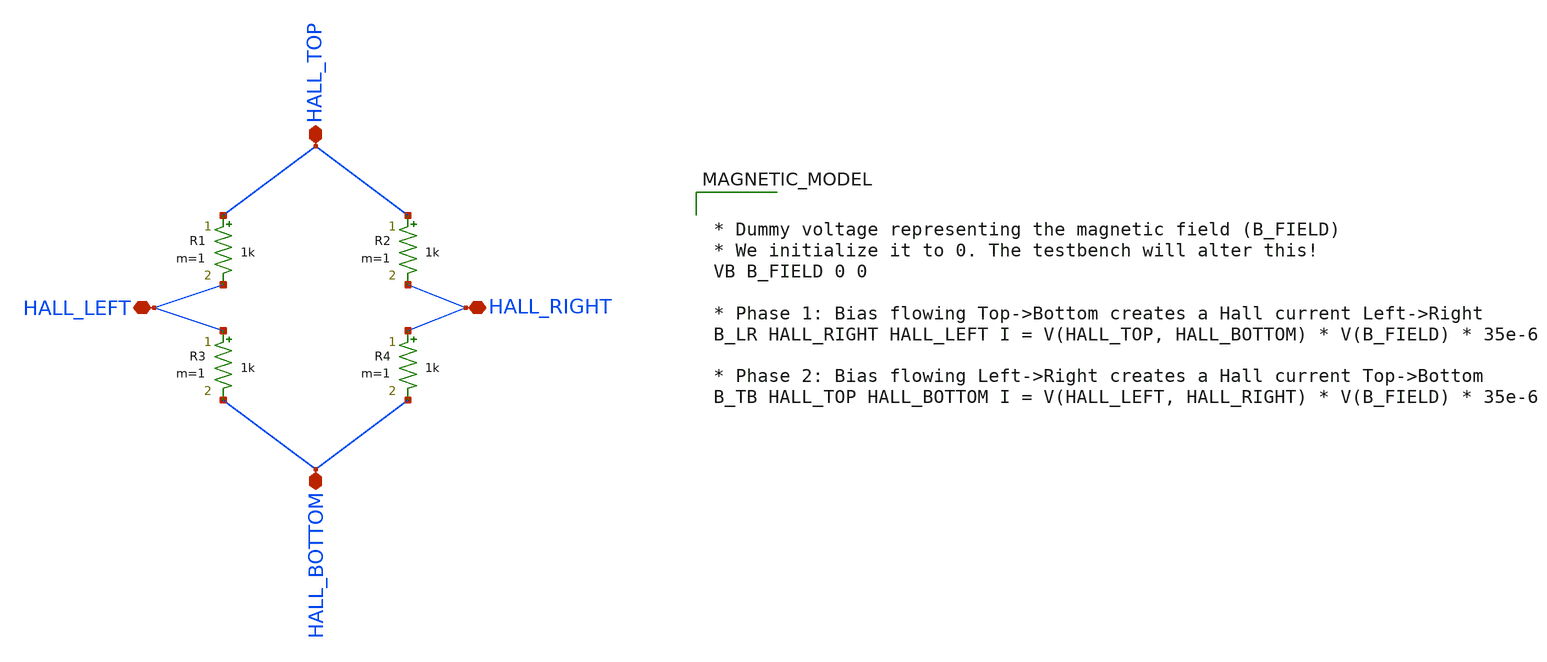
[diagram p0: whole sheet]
** sch_path: xschem/Hall_Sensor.sch
**.subckt Hall_Sensor HALL_TOP HALL_BOTTOM HALL_LEFT HALL_RIGHT
*.iopin HALL_TOP
*.iopin HALL_BOTTOM
*.iopin HALL_LEFT
*.iopin HALL_RIGHT
R1 HALL_TOP HALL_LEFT 1k m=1
R2 HALL_TOP HALL_RIGHT 1k m=1
R3 HALL_LEFT HALL_BOTTOM 1k m=1
R4 HALL_RIGHT HALL_BOTTOM 1k m=1
**** begin user architecture code


* Dummy voltage representing the magnetic field (B_FIELD)
* We initialize it to 0. The testbench will alter this!
VB B_FIELD 0 0

* Phase 1: Bias flowing Top->Bottom creates a Hall current Left->Right
B_LR HALL_RIGHT HALL_LEFT I = V(HALL_TOP, HALL_BOTTOM) * V(B_FIELD) * 35e-6

* Phase 2: Bias flowing Left->Right creates a Hall current Top->Bottom
B_TB HALL_TOP HALL_BOTTOM I = V(HALL_LEFT, HALL_RIGHT) * V(B_FIELD) * 35e-6


**** end user architecture code
**.ends
.end
